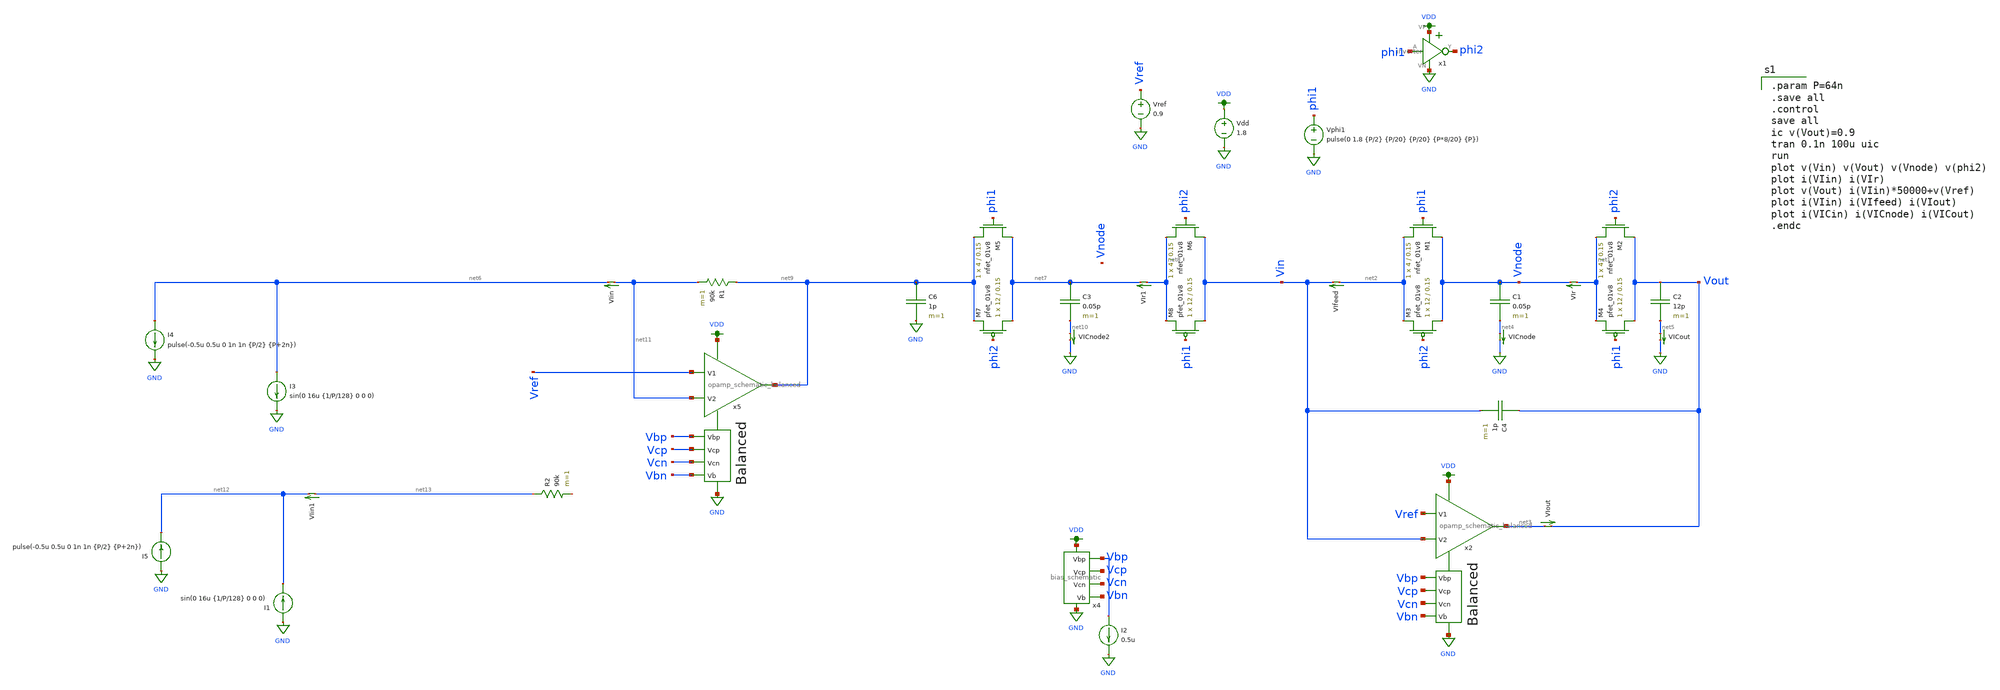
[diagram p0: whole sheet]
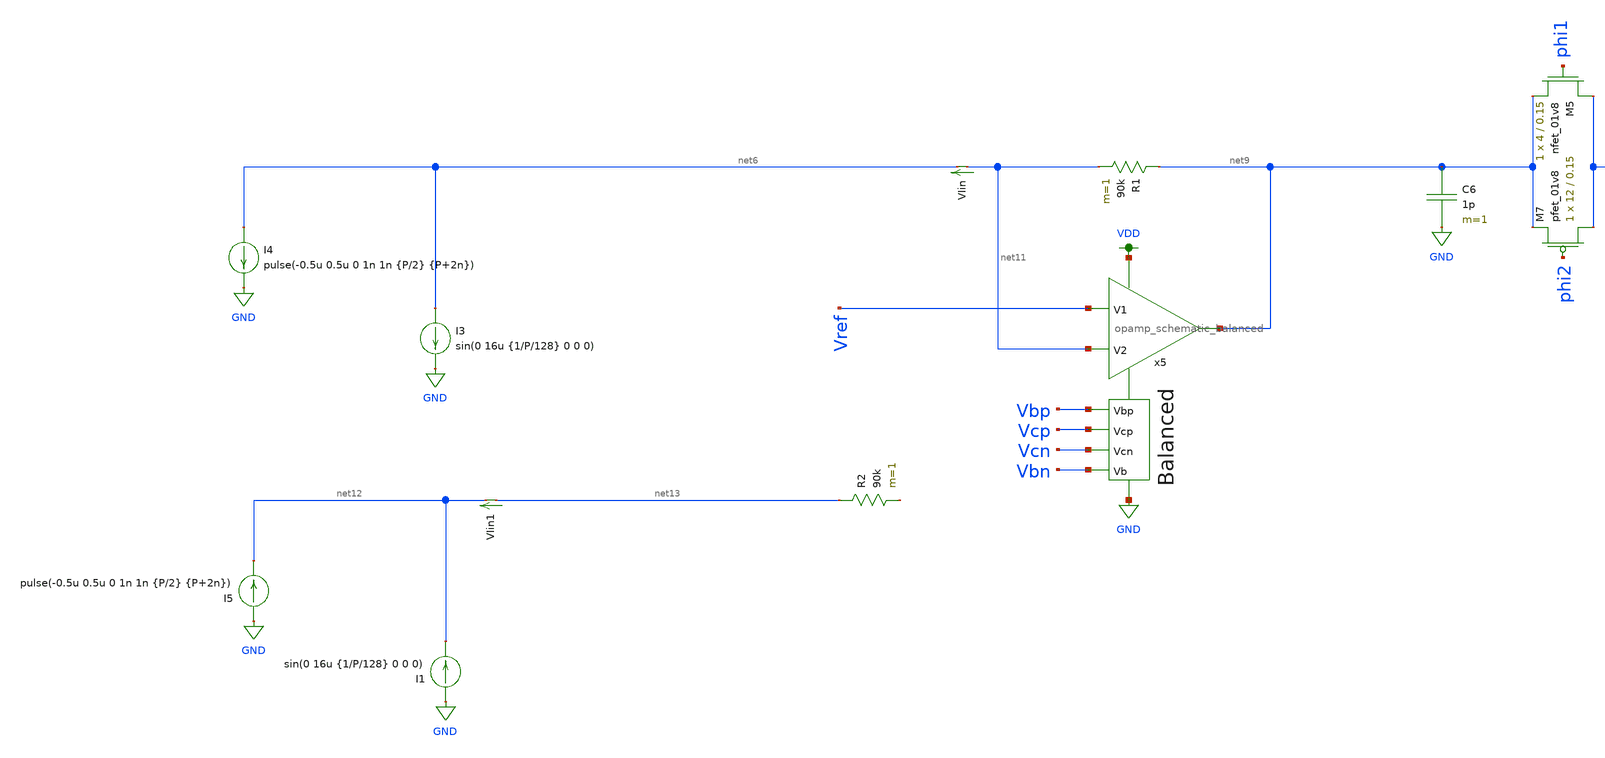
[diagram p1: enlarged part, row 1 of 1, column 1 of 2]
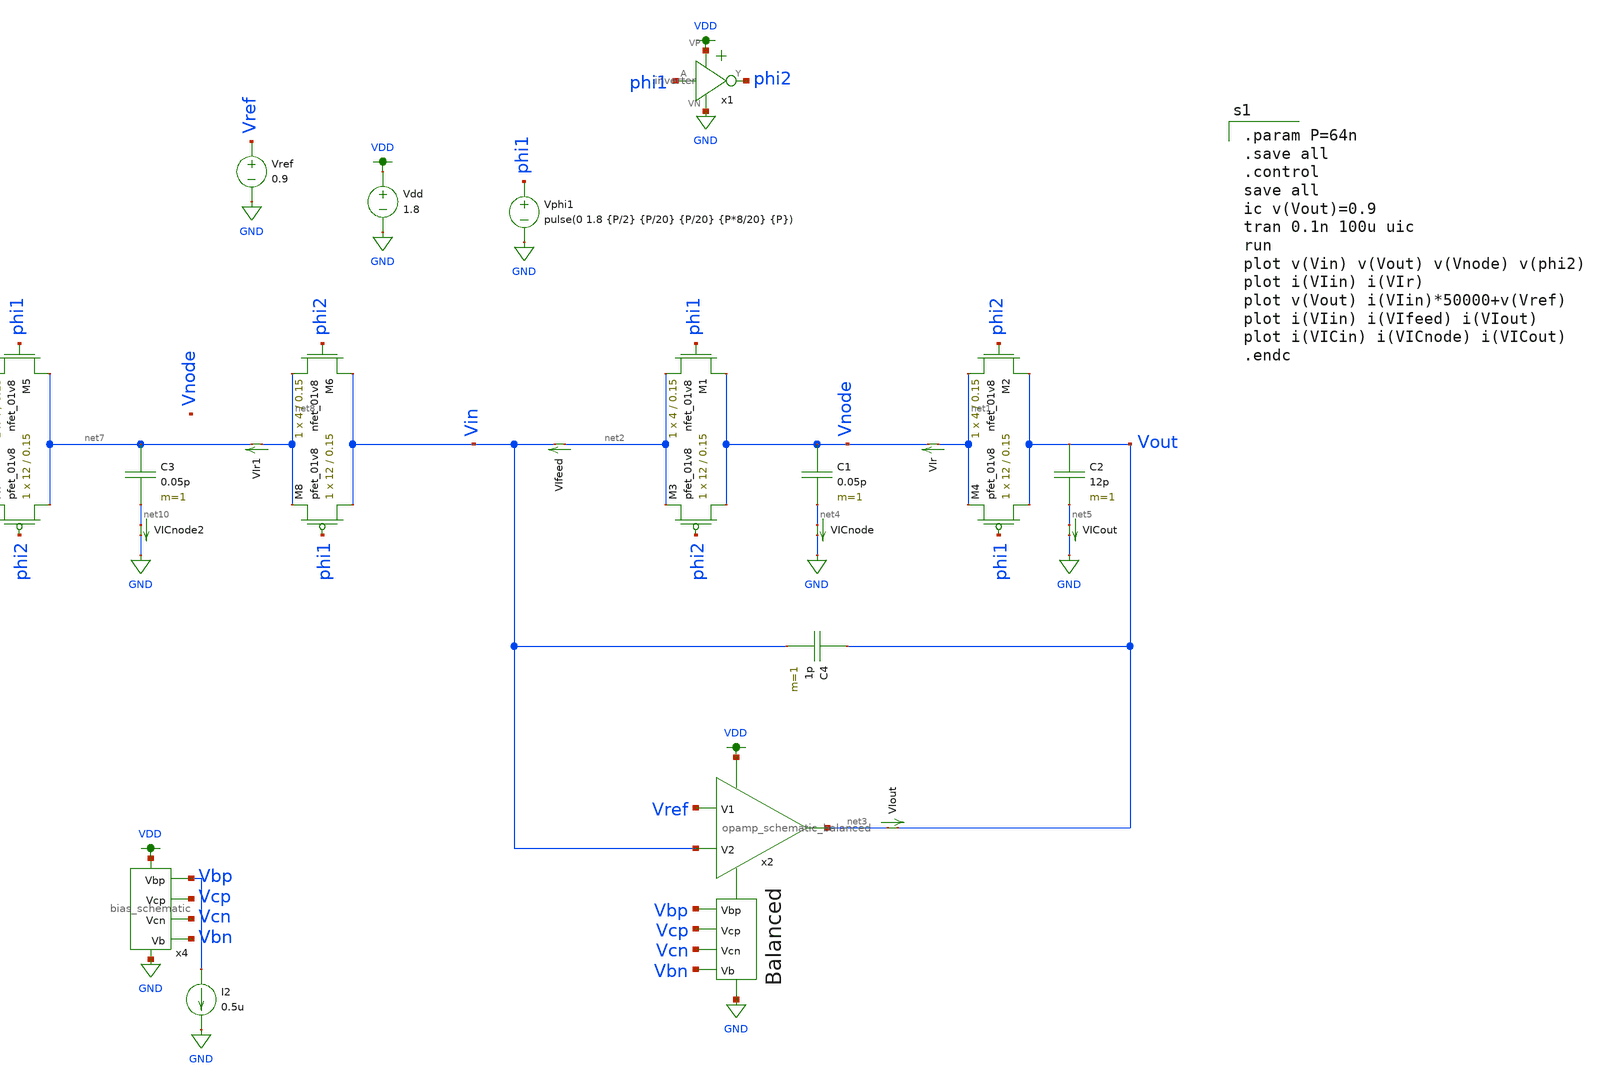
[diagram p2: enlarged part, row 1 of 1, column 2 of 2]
** sch_path: xschem/switched_capacitor/switched_capacitor_iv_lpf_third_order_diff_input.sch
**.subckt switched_capacitor_iv_lpf_third_order_diff_input
C1 Vnode net4 0.05p m=1
XM1 Vnode phi1 net2 GND sky130_fd_pr__nfet_01v8 L=0.15 W=4 nf=1 ad='int((nf+1)/2) * W/nf * 0.29' as='int((nf+2)/2) * W/nf * 0.29'
+ pd='2*int((nf+1)/2) * (W/nf + 0.29)' ps='2*int((nf+2)/2) * (W/nf + 0.29)' nrd='0.29 / W' nrs='0.29 / W'
+ sa=0 sb=0 sd=0 mult=1 m=1
XM2 Vout phi2 net1 GND sky130_fd_pr__nfet_01v8 L=0.15 W=4 nf=1 ad='int((nf+1)/2) * W/nf * 0.29' as='int((nf+2)/2) * W/nf * 0.29'
+ pd='2*int((nf+1)/2) * (W/nf + 0.29)' ps='2*int((nf+2)/2) * (W/nf + 0.29)' nrd='0.29 / W' nrs='0.29 / W'
+ sa=0 sb=0 sd=0 mult=1 m=1
Vphi1 phi1 GND pulse(0 1.8 {P/2} {P/20} {P/20} {P*8/20} {P})
Vdd VDD GND 1.8
C2 Vout net5 12p m=1
XM3 Vnode phi2 net2 VDD sky130_fd_pr__pfet_01v8 L=0.15 W=12 nf=1 ad='int((nf+1)/2) * W/nf * 0.29' as='int((nf+2)/2) * W/nf * 0.29'
+ pd='2*int((nf+1)/2) * (W/nf + 0.29)' ps='2*int((nf+2)/2) * (W/nf + 0.29)' nrd='0.29 / W' nrs='0.29 / W'
+ sa=0 sb=0 sd=0 mult=1 m=1
XM4 Vout phi1 net1 VDD sky130_fd_pr__pfet_01v8 L=0.15 W=12 nf=1 ad='int((nf+1)/2) * W/nf * 0.29' as='int((nf+2)/2) * W/nf * 0.29'
+ pd='2*int((nf+1)/2) * (W/nf + 0.29)' ps='2*int((nf+2)/2) * (W/nf + 0.29)' nrd='0.29 / W' nrs='0.29 / W'
+ sa=0 sb=0 sd=0 mult=1 m=1
x1 VDD phi1 phi2 GND inverter
x4 VDD Vbp Vcp Vcn GND Vbn bias_schematic
Vref Vref GND 0.9
I2 Vbp GND 0.5u
VIin net11 net6 0
.save i(viin)
VIr net1 Vnode 0
.save i(vir)
VIout net3 Vout 0
.save i(viout)
VICnode net4 GND 0
.save i(vicnode)
VICout net5 GND 0
.save i(vicout)
VIfeed net2 Vin 0
.save i(vifeed)
C4 Vout Vin 1p m=1
x2 VDD Vbp Vcp net3 Vref Vin Vcn Vbn GND opamp_schematic_balanced
I3 net6 GND sin(0 16u {1/P/128} 0 0 0)
C3 net7 net10 0.05p m=1
XM5 net7 phi1 net9 GND sky130_fd_pr__nfet_01v8 L=0.15 W=4 nf=1 ad='int((nf+1)/2) * W/nf * 0.29' as='int((nf+2)/2) * W/nf * 0.29'
+ pd='2*int((nf+1)/2) * (W/nf + 0.29)' ps='2*int((nf+2)/2) * (W/nf + 0.29)' nrd='0.29 / W' nrs='0.29 / W'
+ sa=0 sb=0 sd=0 mult=1 m=1
XM6 Vin phi2 net8 GND sky130_fd_pr__nfet_01v8 L=0.15 W=4 nf=1 ad='int((nf+1)/2) * W/nf * 0.29' as='int((nf+2)/2) * W/nf * 0.29'
+ pd='2*int((nf+1)/2) * (W/nf + 0.29)' ps='2*int((nf+2)/2) * (W/nf + 0.29)' nrd='0.29 / W' nrs='0.29 / W'
+ sa=0 sb=0 sd=0 mult=1 m=1
XM7 net7 phi2 net9 VDD sky130_fd_pr__pfet_01v8 L=0.15 W=12 nf=1 ad='int((nf+1)/2) * W/nf * 0.29' as='int((nf+2)/2) * W/nf * 0.29'
+ pd='2*int((nf+1)/2) * (W/nf + 0.29)' ps='2*int((nf+2)/2) * (W/nf + 0.29)' nrd='0.29 / W' nrs='0.29 / W'
+ sa=0 sb=0 sd=0 mult=1 m=1
XM8 Vin phi1 net8 VDD sky130_fd_pr__pfet_01v8 L=0.15 W=12 nf=1 ad='int((nf+1)/2) * W/nf * 0.29' as='int((nf+2)/2) * W/nf * 0.29'
+ pd='2*int((nf+1)/2) * (W/nf + 0.29)' ps='2*int((nf+2)/2) * (W/nf + 0.29)' nrd='0.29 / W' nrs='0.29 / W'
+ sa=0 sb=0 sd=0 mult=1 m=1
VIr1 net8 net7 0
.save i(vir1)
VICnode2 net10 GND 0
.save i(vicnode2)
C6 net9 GND 1p m=1
I4 net6 GND pulse(-0.5u 0.5u 0 1n 1n {P/2} {P+2n})
x5 VDD Vbp Vcp net9 Vref net11 Vcn Vbn GND opamp_schematic_balanced
R1 net9 net11 90k m=1
I1 GND net12 sin(0 16u {1/P/128} 0 0 0)
I5 GND net12 pulse(-0.5u 0.5u 0 1n 1n {P/2} {P+2n})
R2 net13 net14 90k m=1
VIin1 net13 net12 0
.save i(viin1)
**** begin user architecture code

.option wnflag=1
.param MC_SWITCH=0.0
.lib ~/skywater/skywater-pdk/libraries/sky130_fd_pr_ngspice/latest/models/sky130.lib.spice tt


.param P=64n
.save all
.control
save all
ic v(Vout)=0.9
tran 0.1n 100u uic
run
plot v(Vin) v(Vout) v(Vnode) v(phi2)
plot i(VIin) i(VIr)
plot v(Vout) i(VIin)*50000+v(Vref)
plot i(VIin) i(VIfeed) i(VIout)
plot i(VICin) i(VICnode) i(VICout)
.endc

**** end user architecture code
**.ends

* expanding   symbol:  /home/madvlsi/dev/git/magic-dds/xschem/other_project_files/inverter.sym # of
*+ pins=4
** sym_path: xschem/other_project_files/inverter.sym
** sch_path: xschem/other_project_files/inverter.sch
.subckt inverter VP A Y VN
*.iopin VP
*.iopin VN
*.ipin A
*.opin Y
XM1 Y A VN VN sky130_fd_pr__nfet_01v8 L=0.15 W=1 nf=1 ad='int((nf+1)/2) * W/nf * 0.29' as='int((nf+2)/2) * W/nf * 0.29'
+ pd='2*int((nf+1)/2) * (W/nf + 0.29)' ps='2*int((nf+2)/2) * (W/nf + 0.29)' nrd='0.29 / W' nrs='0.29 / W'
+ sa=0 sb=0 sd=0 mult=1 m=1
XM2 Y A VP VP sky130_fd_pr__pfet_01v8 L=0.15 W=4 nf=1 ad='int((nf+1)/2) * W/nf * 0.29' as='int((nf+2)/2) * W/nf * 0.29'
+ pd='2*int((nf+1)/2) * (W/nf + 0.29)' ps='2*int((nf+2)/2) * (W/nf + 0.29)' nrd='0.29 / W' nrs='0.29 / W'
+ sa=0 sb=0 sd=0 mult=1 m=1
.ends


* expanding   symbol:  /home/madvlsi/dev/git/magic-dds/xschem/other_project_files/bias_schematic.sym
*+ # of pins=6
** sym_path: xschem/other_project_files/bias_schematic.sym
** sch_path: xschem/other_project_files/bias_schematic.sch
.subckt bias_schematic VP Vbp Vcp Vcn VN Vb
*.iopin VP
*.iopin VN
*.opin Vcp
*.iopin Vbp
*.opin Vcn
*.opin Vb
XM1a net2 net2 net1 GND sky130_fd_pr__nfet_01v8 L=0.5 W=3 nf=1 ad='int((nf+1)/2) * W/nf * 0.29' as='int((nf+2)/2) * W/nf * 0.29'
+ pd='2*int((nf+1)/2) * (W/nf + 0.29)' ps='2*int((nf+2)/2) * (W/nf + 0.29)' nrd='0.29 / W' nrs='0.29 / W'
+ sa=0 sb=0 sd=0 mult=1 m=1
XM1b net2 net2 net1 GND sky130_fd_pr__nfet_01v8 L=0.5 W=3 nf=1 ad='int((nf+1)/2) * W/nf * 0.29' as='int((nf+2)/2) * W/nf * 0.29'
+ pd='2*int((nf+1)/2) * (W/nf + 0.29)' ps='2*int((nf+2)/2) * (W/nf + 0.29)' nrd='0.29 / W' nrs='0.29 / W'
+ sa=0 sb=0 sd=0 mult=1 m=1
XM1c net2 net2 net1 GND sky130_fd_pr__nfet_01v8 L=0.5 W=3 nf=1 ad='int((nf+1)/2) * W/nf * 0.29' as='int((nf+2)/2) * W/nf * 0.29'
+ pd='2*int((nf+1)/2) * (W/nf + 0.29)' ps='2*int((nf+2)/2) * (W/nf + 0.29)' nrd='0.29 / W' nrs='0.29 / W'
+ sa=0 sb=0 sd=0 mult=1 m=1
XM1d net2 net2 net1 GND sky130_fd_pr__nfet_01v8 L=0.5 W=3 nf=1 ad='int((nf+1)/2) * W/nf * 0.29' as='int((nf+2)/2) * W/nf * 0.29'
+ pd='2*int((nf+1)/2) * (W/nf + 0.29)' ps='2*int((nf+2)/2) * (W/nf + 0.29)' nrd='0.29 / W' nrs='0.29 / W'
+ sa=0 sb=0 sd=0 mult=1 m=1
XM2a VN net2 net1 GND sky130_fd_pr__nfet_01v8 L=0.5 W=3 nf=1 ad='int((nf+1)/2) * W/nf * 0.29' as='int((nf+2)/2) * W/nf * 0.29'
+ pd='2*int((nf+1)/2) * (W/nf + 0.29)' ps='2*int((nf+2)/2) * (W/nf + 0.29)' nrd='0.29 / W' nrs='0.29 / W'
+ sa=0 sb=0 sd=0 mult=1 m=1
XM2b VN net2 net1 GND sky130_fd_pr__nfet_01v8 L=0.5 W=3 nf=1 ad='int((nf+1)/2) * W/nf * 0.29' as='int((nf+2)/2) * W/nf * 0.29'
+ pd='2*int((nf+1)/2) * (W/nf + 0.29)' ps='2*int((nf+2)/2) * (W/nf + 0.29)' nrd='0.29 / W' nrs='0.29 / W'
+ sa=0 sb=0 sd=0 mult=1 m=1
XM2c VN net2 net1 GND sky130_fd_pr__nfet_01v8 L=0.5 W=3 nf=1 ad='int((nf+1)/2) * W/nf * 0.29' as='int((nf+2)/2) * W/nf * 0.29'
+ pd='2*int((nf+1)/2) * (W/nf + 0.29)' ps='2*int((nf+2)/2) * (W/nf + 0.29)' nrd='0.29 / W' nrs='0.29 / W'
+ sa=0 sb=0 sd=0 mult=1 m=1
XM2d VN net2 net1 GND sky130_fd_pr__nfet_01v8 L=0.5 W=3 nf=1 ad='int((nf+1)/2) * W/nf * 0.29' as='int((nf+2)/2) * W/nf * 0.29'
+ pd='2*int((nf+1)/2) * (W/nf + 0.29)' ps='2*int((nf+2)/2) * (W/nf + 0.29)' nrd='0.29 / W' nrs='0.29 / W'
+ sa=0 sb=0 sd=0 mult=1 m=1
XM3a net2 Vbp net7 VDD sky130_fd_pr__pfet_01v8 L=0.5 W=3 nf=1 ad='int((nf+1)/2) * W/nf * 0.29' as='int((nf+2)/2) * W/nf * 0.29'
+ pd='2*int((nf+1)/2) * (W/nf + 0.29)' ps='2*int((nf+2)/2) * (W/nf + 0.29)' nrd='0.29 / W' nrs='0.29 / W'
+ sa=0 sb=0 sd=0 mult=1 m=1
XM3b net7 Vbp net6 VDD sky130_fd_pr__pfet_01v8 L=0.5 W=3 nf=1 ad='int((nf+1)/2) * W/nf * 0.29' as='int((nf+2)/2) * W/nf * 0.29'
+ pd='2*int((nf+1)/2) * (W/nf + 0.29)' ps='2*int((nf+2)/2) * (W/nf + 0.29)' nrd='0.29 / W' nrs='0.29 / W'
+ sa=0 sb=0 sd=0 mult=1 m=1
XM3c net6 Vbp net5 VDD sky130_fd_pr__pfet_01v8 L=0.5 W=3 nf=1 ad='int((nf+1)/2) * W/nf * 0.29' as='int((nf+2)/2) * W/nf * 0.29'
+ pd='2*int((nf+1)/2) * (W/nf + 0.29)' ps='2*int((nf+2)/2) * (W/nf + 0.29)' nrd='0.29 / W' nrs='0.29 / W'
+ sa=0 sb=0 sd=0 mult=1 m=1
XM3d net5 Vbp VP VDD sky130_fd_pr__pfet_01v8 L=0.5 W=3 nf=1 ad='int((nf+1)/2) * W/nf * 0.29' as='int((nf+2)/2) * W/nf * 0.29'
+ pd='2*int((nf+1)/2) * (W/nf + 0.29)' ps='2*int((nf+2)/2) * (W/nf + 0.29)' nrd='0.29 / W' nrs='0.29 / W'
+ sa=0 sb=0 sd=0 mult=1 m=1
XM4a Vcn Vbp VP VDD sky130_fd_pr__pfet_01v8 L=0.5 W=3 nf=1 ad='int((nf+1)/2) * W/nf * 0.29' as='int((nf+2)/2) * W/nf * 0.29'
+ pd='2*int((nf+1)/2) * (W/nf + 0.29)' ps='2*int((nf+2)/2) * (W/nf + 0.29)' nrd='0.29 / W' nrs='0.29 / W'
+ sa=0 sb=0 sd=0 mult=1 m=1
XM4b Vcn Vbp VP VDD sky130_fd_pr__pfet_01v8 L=0.5 W=3 nf=1 ad='int((nf+1)/2) * W/nf * 0.29' as='int((nf+2)/2) * W/nf * 0.29'
+ pd='2*int((nf+1)/2) * (W/nf + 0.29)' ps='2*int((nf+2)/2) * (W/nf + 0.29)' nrd='0.29 / W' nrs='0.29 / W'
+ sa=0 sb=0 sd=0 mult=1 m=1
XM4c Vcn Vbp VP VDD sky130_fd_pr__pfet_01v8 L=0.5 W=3 nf=1 ad='int((nf+1)/2) * W/nf * 0.29' as='int((nf+2)/2) * W/nf * 0.29'
+ pd='2*int((nf+1)/2) * (W/nf + 0.29)' ps='2*int((nf+2)/2) * (W/nf + 0.29)' nrd='0.29 / W' nrs='0.29 / W'
+ sa=0 sb=0 sd=0 mult=1 m=1
XM4d Vcn Vbp VP VDD sky130_fd_pr__pfet_01v8 L=0.5 W=3 nf=1 ad='int((nf+1)/2) * W/nf * 0.29' as='int((nf+2)/2) * W/nf * 0.29'
+ pd='2*int((nf+1)/2) * (W/nf + 0.29)' ps='2*int((nf+2)/2) * (W/nf + 0.29)' nrd='0.29 / W' nrs='0.29 / W'
+ sa=0 sb=0 sd=0 mult=1 m=1
XM11a VP Vbp Vbp VDD sky130_fd_pr__pfet_01v8 L=0.5 W=3 nf=1 ad='int((nf+1)/2) * W/nf * 0.29' as='int((nf+2)/2) * W/nf * 0.29'
+ pd='2*int((nf+1)/2) * (W/nf + 0.29)' ps='2*int((nf+2)/2) * (W/nf + 0.29)' nrd='0.29 / W' nrs='0.29 / W'
+ sa=0 sb=0 sd=0 mult=1 m=1
XM11b VP Vbp Vbp VDD sky130_fd_pr__pfet_01v8 L=0.5 W=3 nf=1 ad='int((nf+1)/2) * W/nf * 0.29' as='int((nf+2)/2) * W/nf * 0.29'
+ pd='2*int((nf+1)/2) * (W/nf + 0.29)' ps='2*int((nf+2)/2) * (W/nf + 0.29)' nrd='0.29 / W' nrs='0.29 / W'
+ sa=0 sb=0 sd=0 mult=1 m=1
XM11c VP Vbp Vbp VDD sky130_fd_pr__pfet_01v8 L=0.5 W=3 nf=1 ad='int((nf+1)/2) * W/nf * 0.29' as='int((nf+2)/2) * W/nf * 0.29'
+ pd='2*int((nf+1)/2) * (W/nf + 0.29)' ps='2*int((nf+2)/2) * (W/nf + 0.29)' nrd='0.29 / W' nrs='0.29 / W'
+ sa=0 sb=0 sd=0 mult=1 m=1
XM11d VP Vbp Vbp VDD sky130_fd_pr__pfet_01v8 L=0.5 W=3 nf=1 ad='int((nf+1)/2) * W/nf * 0.29' as='int((nf+2)/2) * W/nf * 0.29'
+ pd='2*int((nf+1)/2) * (W/nf + 0.29)' ps='2*int((nf+2)/2) * (W/nf + 0.29)' nrd='0.29 / W' nrs='0.29 / W'
+ sa=0 sb=0 sd=0 mult=1 m=1
XM5a net1 Vcn Vcn GND sky130_fd_pr__nfet_01v8 L=0.5 W=3 nf=1 ad='int((nf+1)/2) * W/nf * 0.29' as='int((nf+2)/2) * W/nf * 0.29'
+ pd='2*int((nf+1)/2) * (W/nf + 0.29)' ps='2*int((nf+2)/2) * (W/nf + 0.29)' nrd='0.29 / W' nrs='0.29 / W'
+ sa=0 sb=0 sd=0 mult=1 m=1
XM5b net1 Vcn Vcn GND sky130_fd_pr__nfet_01v8 L=0.5 W=3 nf=1 ad='int((nf+1)/2) * W/nf * 0.29' as='int((nf+2)/2) * W/nf * 0.29'
+ pd='2*int((nf+1)/2) * (W/nf + 0.29)' ps='2*int((nf+2)/2) * (W/nf + 0.29)' nrd='0.29 / W' nrs='0.29 / W'
+ sa=0 sb=0 sd=0 mult=1 m=1
XM5c net1 Vcn Vcn GND sky130_fd_pr__nfet_01v8 L=0.5 W=3 nf=1 ad='int((nf+1)/2) * W/nf * 0.29' as='int((nf+2)/2) * W/nf * 0.29'
+ pd='2*int((nf+1)/2) * (W/nf + 0.29)' ps='2*int((nf+2)/2) * (W/nf + 0.29)' nrd='0.29 / W' nrs='0.29 / W'
+ sa=0 sb=0 sd=0 mult=1 m=1
XM5d net1 Vcn Vcn GND sky130_fd_pr__nfet_01v8 L=0.5 W=3 nf=1 ad='int((nf+1)/2) * W/nf * 0.29' as='int((nf+2)/2) * W/nf * 0.29'
+ pd='2*int((nf+1)/2) * (W/nf + 0.29)' ps='2*int((nf+2)/2) * (W/nf + 0.29)' nrd='0.29 / W' nrs='0.29 / W'
+ sa=0 sb=0 sd=0 mult=1 m=1
XM8a net10 Vb net3 GND sky130_fd_pr__nfet_01v8 L=0.5 W=3 nf=1 ad='int((nf+1)/2) * W/nf * 0.29' as='int((nf+2)/2) * W/nf * 0.29'
+ pd='2*int((nf+1)/2) * (W/nf + 0.29)' ps='2*int((nf+2)/2) * (W/nf + 0.29)' nrd='0.29 / W' nrs='0.29 / W'
+ sa=0 sb=0 sd=0 mult=1 m=1
XM8b net9 Vb net10 GND sky130_fd_pr__nfet_01v8 L=0.5 W=3 nf=1 ad='int((nf+1)/2) * W/nf * 0.29' as='int((nf+2)/2) * W/nf * 0.29'
+ pd='2*int((nf+1)/2) * (W/nf + 0.29)' ps='2*int((nf+2)/2) * (W/nf + 0.29)' nrd='0.29 / W' nrs='0.29 / W'
+ sa=0 sb=0 sd=0 mult=1 m=1
XM8c net8 Vb net9 GND sky130_fd_pr__nfet_01v8 L=0.5 W=3 nf=1 ad='int((nf+1)/2) * W/nf * 0.29' as='int((nf+2)/2) * W/nf * 0.29'
+ pd='2*int((nf+1)/2) * (W/nf + 0.29)' ps='2*int((nf+2)/2) * (W/nf + 0.29)' nrd='0.29 / W' nrs='0.29 / W'
+ sa=0 sb=0 sd=0 mult=1 m=1
XM8d VN Vb net8 GND sky130_fd_pr__nfet_01v8 L=0.5 W=3 nf=1 ad='int((nf+1)/2) * W/nf * 0.29' as='int((nf+2)/2) * W/nf * 0.29'
+ pd='2*int((nf+1)/2) * (W/nf + 0.29)' ps='2*int((nf+2)/2) * (W/nf + 0.29)' nrd='0.29 / W' nrs='0.29 / W'
+ sa=0 sb=0 sd=0 mult=1 m=1
XM6a net3 net3 net4 VDD sky130_fd_pr__pfet_01v8 L=0.5 W=3 nf=1 ad='int((nf+1)/2) * W/nf * 0.29' as='int((nf+2)/2) * W/nf * 0.29'
+ pd='2*int((nf+1)/2) * (W/nf + 0.29)' ps='2*int((nf+2)/2) * (W/nf + 0.29)' nrd='0.29 / W' nrs='0.29 / W'
+ sa=0 sb=0 sd=0 mult=1 m=1
XM6b net3 net3 net4 VDD sky130_fd_pr__pfet_01v8 L=0.5 W=3 nf=1 ad='int((nf+1)/2) * W/nf * 0.29' as='int((nf+2)/2) * W/nf * 0.29'
+ pd='2*int((nf+1)/2) * (W/nf + 0.29)' ps='2*int((nf+2)/2) * (W/nf + 0.29)' nrd='0.29 / W' nrs='0.29 / W'
+ sa=0 sb=0 sd=0 mult=1 m=1
XM6c net3 net3 net4 VDD sky130_fd_pr__pfet_01v8 L=0.5 W=3 nf=1 ad='int((nf+1)/2) * W/nf * 0.29' as='int((nf+2)/2) * W/nf * 0.29'
+ pd='2*int((nf+1)/2) * (W/nf + 0.29)' ps='2*int((nf+2)/2) * (W/nf + 0.29)' nrd='0.29 / W' nrs='0.29 / W'
+ sa=0 sb=0 sd=0 mult=1 m=1
XM6d net3 net3 net4 VDD sky130_fd_pr__pfet_01v8 L=0.5 W=3 nf=1 ad='int((nf+1)/2) * W/nf * 0.29' as='int((nf+2)/2) * W/nf * 0.29'
+ pd='2*int((nf+1)/2) * (W/nf + 0.29)' ps='2*int((nf+2)/2) * (W/nf + 0.29)' nrd='0.29 / W' nrs='0.29 / W'
+ sa=0 sb=0 sd=0 mult=1 m=1
XM7a net4 net3 VP VDD sky130_fd_pr__pfet_01v8 L=0.5 W=3 nf=1 ad='int((nf+1)/2) * W/nf * 0.29' as='int((nf+2)/2) * W/nf * 0.29'
+ pd='2*int((nf+1)/2) * (W/nf + 0.29)' ps='2*int((nf+2)/2) * (W/nf + 0.29)' nrd='0.29 / W' nrs='0.29 / W'
+ sa=0 sb=0 sd=0 mult=1 m=1
XM7b net4 net3 VP VDD sky130_fd_pr__pfet_01v8 L=0.5 W=3 nf=1 ad='int((nf+1)/2) * W/nf * 0.29' as='int((nf+2)/2) * W/nf * 0.29'
+ pd='2*int((nf+1)/2) * (W/nf + 0.29)' ps='2*int((nf+2)/2) * (W/nf + 0.29)' nrd='0.29 / W' nrs='0.29 / W'
+ sa=0 sb=0 sd=0 mult=1 m=1
XM7c net4 net3 VP VDD sky130_fd_pr__pfet_01v8 L=0.5 W=3 nf=1 ad='int((nf+1)/2) * W/nf * 0.29' as='int((nf+2)/2) * W/nf * 0.29'
+ pd='2*int((nf+1)/2) * (W/nf + 0.29)' ps='2*int((nf+2)/2) * (W/nf + 0.29)' nrd='0.29 / W' nrs='0.29 / W'
+ sa=0 sb=0 sd=0 mult=1 m=1
XM7d net4 net3 VP VDD sky130_fd_pr__pfet_01v8 L=0.5 W=3 nf=1 ad='int((nf+1)/2) * W/nf * 0.29' as='int((nf+2)/2) * W/nf * 0.29'
+ pd='2*int((nf+1)/2) * (W/nf + 0.29)' ps='2*int((nf+2)/2) * (W/nf + 0.29)' nrd='0.29 / W' nrs='0.29 / W'
+ sa=0 sb=0 sd=0 mult=1 m=1
XM10d net4 Vcp Vcp VDD sky130_fd_pr__pfet_01v8 L=0.5 W=3 nf=1 ad='int((nf+1)/2) * W/nf * 0.29' as='int((nf+2)/2) * W/nf * 0.29'
+ pd='2*int((nf+1)/2) * (W/nf + 0.29)' ps='2*int((nf+2)/2) * (W/nf + 0.29)' nrd='0.29 / W' nrs='0.29 / W'
+ sa=0 sb=0 sd=0 mult=1 m=1
XM10c net4 Vcp Vcp VDD sky130_fd_pr__pfet_01v8 L=0.5 W=3 nf=1 ad='int((nf+1)/2) * W/nf * 0.29' as='int((nf+2)/2) * W/nf * 0.29'
+ pd='2*int((nf+1)/2) * (W/nf + 0.29)' ps='2*int((nf+2)/2) * (W/nf + 0.29)' nrd='0.29 / W' nrs='0.29 / W'
+ sa=0 sb=0 sd=0 mult=1 m=1
XM10b net4 Vcp Vcp VDD sky130_fd_pr__pfet_01v8 L=0.5 W=3 nf=1 ad='int((nf+1)/2) * W/nf * 0.29' as='int((nf+2)/2) * W/nf * 0.29'
+ pd='2*int((nf+1)/2) * (W/nf + 0.29)' ps='2*int((nf+2)/2) * (W/nf + 0.29)' nrd='0.29 / W' nrs='0.29 / W'
+ sa=0 sb=0 sd=0 mult=1 m=1
XM10a net4 Vcp Vcp VDD sky130_fd_pr__pfet_01v8 L=0.5 W=3 nf=1 ad='int((nf+1)/2) * W/nf * 0.29' as='int((nf+2)/2) * W/nf * 0.29'
+ pd='2*int((nf+1)/2) * (W/nf + 0.29)' ps='2*int((nf+2)/2) * (W/nf + 0.29)' nrd='0.29 / W' nrs='0.29 / W'
+ sa=0 sb=0 sd=0 mult=1 m=1
XM9a VN Vb Vcp GND sky130_fd_pr__nfet_01v8 L=0.5 W=3 nf=1 ad='int((nf+1)/2) * W/nf * 0.29' as='int((nf+2)/2) * W/nf * 0.29'
+ pd='2*int((nf+1)/2) * (W/nf + 0.29)' ps='2*int((nf+2)/2) * (W/nf + 0.29)' nrd='0.29 / W' nrs='0.29 / W'
+ sa=0 sb=0 sd=0 mult=1 m=1
XM9b VN Vb Vcp GND sky130_fd_pr__nfet_01v8 L=0.5 W=3 nf=1 ad='int((nf+1)/2) * W/nf * 0.29' as='int((nf+2)/2) * W/nf * 0.29'
+ pd='2*int((nf+1)/2) * (W/nf + 0.29)' ps='2*int((nf+2)/2) * (W/nf + 0.29)' nrd='0.29 / W' nrs='0.29 / W'
+ sa=0 sb=0 sd=0 mult=1 m=1
XM9c VN Vb Vcp GND sky130_fd_pr__nfet_01v8 L=0.5 W=3 nf=1 ad='int((nf+1)/2) * W/nf * 0.29' as='int((nf+2)/2) * W/nf * 0.29'
+ pd='2*int((nf+1)/2) * (W/nf + 0.29)' ps='2*int((nf+2)/2) * (W/nf + 0.29)' nrd='0.29 / W' nrs='0.29 / W'
+ sa=0 sb=0 sd=0 mult=1 m=1
XM9d VN Vb Vcp GND sky130_fd_pr__nfet_01v8 L=0.5 W=3 nf=1 ad='int((nf+1)/2) * W/nf * 0.29' as='int((nf+2)/2) * W/nf * 0.29'
+ pd='2*int((nf+1)/2) * (W/nf + 0.29)' ps='2*int((nf+2)/2) * (W/nf + 0.29)' nrd='0.29 / W' nrs='0.29 / W'
+ sa=0 sb=0 sd=0 mult=1 m=1
XM12a VN Vb Vb GND sky130_fd_pr__nfet_01v8 L=0.5 W=3 nf=1 ad='int((nf+1)/2) * W/nf * 0.29' as='int((nf+2)/2) * W/nf * 0.29'
+ pd='2*int((nf+1)/2) * (W/nf + 0.29)' ps='2*int((nf+2)/2) * (W/nf + 0.29)' nrd='0.29 / W' nrs='0.29 / W'
+ sa=0 sb=0 sd=0 mult=1 m=1
XM12b VN Vb Vb GND sky130_fd_pr__nfet_01v8 L=0.5 W=3 nf=1 ad='int((nf+1)/2) * W/nf * 0.29' as='int((nf+2)/2) * W/nf * 0.29'
+ pd='2*int((nf+1)/2) * (W/nf + 0.29)' ps='2*int((nf+2)/2) * (W/nf + 0.29)' nrd='0.29 / W' nrs='0.29 / W'
+ sa=0 sb=0 sd=0 mult=1 m=1
XM12c VN Vb Vb GND sky130_fd_pr__nfet_01v8 L=0.5 W=3 nf=1 ad='int((nf+1)/2) * W/nf * 0.29' as='int((nf+2)/2) * W/nf * 0.29'
+ pd='2*int((nf+1)/2) * (W/nf + 0.29)' ps='2*int((nf+2)/2) * (W/nf + 0.29)' nrd='0.29 / W' nrs='0.29 / W'
+ sa=0 sb=0 sd=0 mult=1 m=1
XM12d VN Vb Vb GND sky130_fd_pr__nfet_01v8 L=0.5 W=3 nf=1 ad='int((nf+1)/2) * W/nf * 0.29' as='int((nf+2)/2) * W/nf * 0.29'
+ pd='2*int((nf+1)/2) * (W/nf + 0.29)' ps='2*int((nf+2)/2) * (W/nf + 0.29)' nrd='0.29 / W' nrs='0.29 / W'
+ sa=0 sb=0 sd=0 mult=1 m=1
XM1 Vb Vbp VP VDD sky130_fd_pr__pfet_01v8 L=0.5 W=3 nf=1 ad='int((nf+1)/2) * W/nf * 0.29' as='int((nf+2)/2) * W/nf * 0.29'
+ pd='2*int((nf+1)/2) * (W/nf + 0.29)' ps='2*int((nf+2)/2) * (W/nf + 0.29)' nrd='0.29 / W' nrs='0.29 / W'
+ sa=0 sb=0 sd=0 mult=1 m=1
XM2 Vb Vbp VP VDD sky130_fd_pr__pfet_01v8 L=0.5 W=3 nf=1 ad='int((nf+1)/2) * W/nf * 0.29' as='int((nf+2)/2) * W/nf * 0.29'
+ pd='2*int((nf+1)/2) * (W/nf + 0.29)' ps='2*int((nf+2)/2) * (W/nf + 0.29)' nrd='0.29 / W' nrs='0.29 / W'
+ sa=0 sb=0 sd=0 mult=1 m=1
XM3 Vb Vbp VP VDD sky130_fd_pr__pfet_01v8 L=0.5 W=3 nf=1 ad='int((nf+1)/2) * W/nf * 0.29' as='int((nf+2)/2) * W/nf * 0.29'
+ pd='2*int((nf+1)/2) * (W/nf + 0.29)' ps='2*int((nf+2)/2) * (W/nf + 0.29)' nrd='0.29 / W' nrs='0.29 / W'
+ sa=0 sb=0 sd=0 mult=1 m=1
XM4 Vb Vbp VP VDD sky130_fd_pr__pfet_01v8 L=0.5 W=3 nf=1 ad='int((nf+1)/2) * W/nf * 0.29' as='int((nf+2)/2) * W/nf * 0.29'
+ pd='2*int((nf+1)/2) * (W/nf + 0.29)' ps='2*int((nf+2)/2) * (W/nf + 0.29)' nrd='0.29 / W' nrs='0.29 / W'
+ sa=0 sb=0 sd=0 mult=1 m=1
XM1e net2 net2 net1 GND sky130_fd_pr__nfet_01v8 L=0.5 W=3 nf=1 ad='int((nf+1)/2) * W/nf * 0.29' as='int((nf+2)/2) * W/nf * 0.29'
+ pd='2*int((nf+1)/2) * (W/nf + 0.29)' ps='2*int((nf+2)/2) * (W/nf + 0.29)' nrd='0.29 / W' nrs='0.29 / W'
+ sa=0 sb=0 sd=0 mult=1 m=1
XM1f net2 net2 net1 GND sky130_fd_pr__nfet_01v8 L=0.5 W=3 nf=1 ad='int((nf+1)/2) * W/nf * 0.29' as='int((nf+2)/2) * W/nf * 0.29'
+ pd='2*int((nf+1)/2) * (W/nf + 0.29)' ps='2*int((nf+2)/2) * (W/nf + 0.29)' nrd='0.29 / W' nrs='0.29 / W'
+ sa=0 sb=0 sd=0 mult=1 m=1
XM1g net2 net2 net1 GND sky130_fd_pr__nfet_01v8 L=0.5 W=3 nf=1 ad='int((nf+1)/2) * W/nf * 0.29' as='int((nf+2)/2) * W/nf * 0.29'
+ pd='2*int((nf+1)/2) * (W/nf + 0.29)' ps='2*int((nf+2)/2) * (W/nf + 0.29)' nrd='0.29 / W' nrs='0.29 / W'
+ sa=0 sb=0 sd=0 mult=1 m=1
XM1h net2 net2 net1 GND sky130_fd_pr__nfet_01v8 L=0.5 W=3 nf=1 ad='int((nf+1)/2) * W/nf * 0.29' as='int((nf+2)/2) * W/nf * 0.29'
+ pd='2*int((nf+1)/2) * (W/nf + 0.29)' ps='2*int((nf+2)/2) * (W/nf + 0.29)' nrd='0.29 / W' nrs='0.29 / W'
+ sa=0 sb=0 sd=0 mult=1 m=1
XM6e net3 net3 net4 VDD sky130_fd_pr__pfet_01v8 L=0.5 W=3 nf=1 ad='int((nf+1)/2) * W/nf * 0.29' as='int((nf+2)/2) * W/nf * 0.29'
+ pd='2*int((nf+1)/2) * (W/nf + 0.29)' ps='2*int((nf+2)/2) * (W/nf + 0.29)' nrd='0.29 / W' nrs='0.29 / W'
+ sa=0 sb=0 sd=0 mult=1 m=1
XM6f net3 net3 net4 VDD sky130_fd_pr__pfet_01v8 L=0.5 W=3 nf=1 ad='int((nf+1)/2) * W/nf * 0.29' as='int((nf+2)/2) * W/nf * 0.29'
+ pd='2*int((nf+1)/2) * (W/nf + 0.29)' ps='2*int((nf+2)/2) * (W/nf + 0.29)' nrd='0.29 / W' nrs='0.29 / W'
+ sa=0 sb=0 sd=0 mult=1 m=1
XM6g net3 net3 net4 VDD sky130_fd_pr__pfet_01v8 L=0.5 W=3 nf=1 ad='int((nf+1)/2) * W/nf * 0.29' as='int((nf+2)/2) * W/nf * 0.29'
+ pd='2*int((nf+1)/2) * (W/nf + 0.29)' ps='2*int((nf+2)/2) * (W/nf + 0.29)' nrd='0.29 / W' nrs='0.29 / W'
+ sa=0 sb=0 sd=0 mult=1 m=1
XM6h net3 net3 net4 VDD sky130_fd_pr__pfet_01v8 L=0.5 W=3 nf=1 ad='int((nf+1)/2) * W/nf * 0.29' as='int((nf+2)/2) * W/nf * 0.29'
+ pd='2*int((nf+1)/2) * (W/nf + 0.29)' ps='2*int((nf+2)/2) * (W/nf + 0.29)' nrd='0.29 / W' nrs='0.29 / W'
+ sa=0 sb=0 sd=0 mult=1 m=1
XM1i net2 net2 net1 GND sky130_fd_pr__nfet_01v8 L=0.5 W=3 nf=1 ad='int((nf+1)/2) * W/nf * 0.29' as='int((nf+2)/2) * W/nf * 0.29'
+ pd='2*int((nf+1)/2) * (W/nf + 0.29)' ps='2*int((nf+2)/2) * (W/nf + 0.29)' nrd='0.29 / W' nrs='0.29 / W'
+ sa=0 sb=0 sd=0 mult=1 m=1
XM1j net2 net2 net1 GND sky130_fd_pr__nfet_01v8 L=0.5 W=3 nf=1 ad='int((nf+1)/2) * W/nf * 0.29' as='int((nf+2)/2) * W/nf * 0.29'
+ pd='2*int((nf+1)/2) * (W/nf + 0.29)' ps='2*int((nf+2)/2) * (W/nf + 0.29)' nrd='0.29 / W' nrs='0.29 / W'
+ sa=0 sb=0 sd=0 mult=1 m=1
XM1k net2 net2 net1 GND sky130_fd_pr__nfet_01v8 L=0.5 W=3 nf=1 ad='int((nf+1)/2) * W/nf * 0.29' as='int((nf+2)/2) * W/nf * 0.29'
+ pd='2*int((nf+1)/2) * (W/nf + 0.29)' ps='2*int((nf+2)/2) * (W/nf + 0.29)' nrd='0.29 / W' nrs='0.29 / W'
+ sa=0 sb=0 sd=0 mult=1 m=1
XM1l net2 net2 net1 GND sky130_fd_pr__nfet_01v8 L=0.5 W=3 nf=1 ad='int((nf+1)/2) * W/nf * 0.29' as='int((nf+2)/2) * W/nf * 0.29'
+ pd='2*int((nf+1)/2) * (W/nf + 0.29)' ps='2*int((nf+2)/2) * (W/nf + 0.29)' nrd='0.29 / W' nrs='0.29 / W'
+ sa=0 sb=0 sd=0 mult=1 m=1
XM6i net3 net3 net4 VDD sky130_fd_pr__pfet_01v8 L=0.5 W=3 nf=1 ad='int((nf+1)/2) * W/nf * 0.29' as='int((nf+2)/2) * W/nf * 0.29'
+ pd='2*int((nf+1)/2) * (W/nf + 0.29)' ps='2*int((nf+2)/2) * (W/nf + 0.29)' nrd='0.29 / W' nrs='0.29 / W'
+ sa=0 sb=0 sd=0 mult=1 m=1
XM6j net3 net3 net4 VDD sky130_fd_pr__pfet_01v8 L=0.5 W=3 nf=1 ad='int((nf+1)/2) * W/nf * 0.29' as='int((nf+2)/2) * W/nf * 0.29'
+ pd='2*int((nf+1)/2) * (W/nf + 0.29)' ps='2*int((nf+2)/2) * (W/nf + 0.29)' nrd='0.29 / W' nrs='0.29 / W'
+ sa=0 sb=0 sd=0 mult=1 m=1
XM6k net3 net3 net4 VDD sky130_fd_pr__pfet_01v8 L=0.5 W=3 nf=1 ad='int((nf+1)/2) * W/nf * 0.29' as='int((nf+2)/2) * W/nf * 0.29'
+ pd='2*int((nf+1)/2) * (W/nf + 0.29)' ps='2*int((nf+2)/2) * (W/nf + 0.29)' nrd='0.29 / W' nrs='0.29 / W'
+ sa=0 sb=0 sd=0 mult=1 m=1
XM6l net3 net3 net4 VDD sky130_fd_pr__pfet_01v8 L=0.5 W=3 nf=1 ad='int((nf+1)/2) * W/nf * 0.29' as='int((nf+2)/2) * W/nf * 0.29'
+ pd='2*int((nf+1)/2) * (W/nf + 0.29)' ps='2*int((nf+2)/2) * (W/nf + 0.29)' nrd='0.29 / W' nrs='0.29 / W'
+ sa=0 sb=0 sd=0 mult=1 m=1
.ends


* expanding   symbol:
*+  /home/madvlsi/dev/git/magic-dds/xschem/other_project_files/opamp_schematic_balanced.sym # of pins=9
** sym_path: xschem/other_project_files/opamp_schematic_balanced.sym
** sch_path: xschem/other_project_files/opamp_schematic_balanced.sch
.subckt opamp_schematic_balanced VP Vbp Vcp Vout V1 V2 Vcn Vb VN
*.ipin Vbp
*.ipin Vcp
*.ipin Vcn
*.ipin V2
*.ipin V1
*.ipin Vb
*.iopin VP
*.iopin VN
*.opin Vout
XM1a M1top V1 Vnode GND sky130_fd_pr__nfet_01v8 L=0.5 W=3 nf=1 ad='int((nf+1)/2) * W/nf * 0.29' as='int((nf+2)/2) * W/nf * 0.29'
+ pd='2*int((nf+1)/2) * (W/nf + 0.29)' ps='2*int((nf+2)/2) * (W/nf + 0.29)' nrd='0.29 / W' nrs='0.29 / W'
+ sa=0 sb=0 sd=0 mult=1 m=1
XM1b M1top V1 Vnode GND sky130_fd_pr__nfet_01v8 L=0.5 W=3 nf=1 ad='int((nf+1)/2) * W/nf * 0.29' as='int((nf+2)/2) * W/nf * 0.29'
+ pd='2*int((nf+1)/2) * (W/nf + 0.29)' ps='2*int((nf+2)/2) * (W/nf + 0.29)' nrd='0.29 / W' nrs='0.29 / W'
+ sa=0 sb=0 sd=0 mult=1 m=1
XM1c M1top V1 Vnode GND sky130_fd_pr__nfet_01v8 L=0.5 W=3 nf=1 ad='int((nf+1)/2) * W/nf * 0.29' as='int((nf+2)/2) * W/nf * 0.29'
+ pd='2*int((nf+1)/2) * (W/nf + 0.29)' ps='2*int((nf+2)/2) * (W/nf + 0.29)' nrd='0.29 / W' nrs='0.29 / W'
+ sa=0 sb=0 sd=0 mult=1 m=1
XM1d M1top V1 Vnode GND sky130_fd_pr__nfet_01v8 L=0.5 W=3 nf=1 ad='int((nf+1)/2) * W/nf * 0.29' as='int((nf+2)/2) * W/nf * 0.29'
+ pd='2*int((nf+1)/2) * (W/nf + 0.29)' ps='2*int((nf+2)/2) * (W/nf + 0.29)' nrd='0.29 / W' nrs='0.29 / W'
+ sa=0 sb=0 sd=0 mult=1 m=1
XM2a M2top V2 Vnode GND sky130_fd_pr__nfet_01v8 L=0.5 W=3 nf=1 ad='int((nf+1)/2) * W/nf * 0.29' as='int((nf+2)/2) * W/nf * 0.29'
+ pd='2*int((nf+1)/2) * (W/nf + 0.29)' ps='2*int((nf+2)/2) * (W/nf + 0.29)' nrd='0.29 / W' nrs='0.29 / W'
+ sa=0 sb=0 sd=0 mult=1 m=1
XM2b M2top V2 Vnode GND sky130_fd_pr__nfet_01v8 L=0.5 W=3 nf=1 ad='int((nf+1)/2) * W/nf * 0.29' as='int((nf+2)/2) * W/nf * 0.29'
+ pd='2*int((nf+1)/2) * (W/nf + 0.29)' ps='2*int((nf+2)/2) * (W/nf + 0.29)' nrd='0.29 / W' nrs='0.29 / W'
+ sa=0 sb=0 sd=0 mult=1 m=1
XM2c M2top V2 Vnode GND sky130_fd_pr__nfet_01v8 L=0.5 W=3 nf=1 ad='int((nf+1)/2) * W/nf * 0.29' as='int((nf+2)/2) * W/nf * 0.29'
+ pd='2*int((nf+1)/2) * (W/nf + 0.29)' ps='2*int((nf+2)/2) * (W/nf + 0.29)' nrd='0.29 / W' nrs='0.29 / W'
+ sa=0 sb=0 sd=0 mult=1 m=1
XM2d M2top V2 Vnode GND sky130_fd_pr__nfet_01v8 L=0.5 W=3 nf=1 ad='int((nf+1)/2) * W/nf * 0.29' as='int((nf+2)/2) * W/nf * 0.29'
+ pd='2*int((nf+1)/2) * (W/nf + 0.29)' ps='2*int((nf+2)/2) * (W/nf + 0.29)' nrd='0.29 / W' nrs='0.29 / W'
+ sa=0 sb=0 sd=0 mult=1 m=1
XMba Vnode Vb VN GND sky130_fd_pr__nfet_01v8 L=0.5 W=1.5 nf=1 ad='int((nf+1)/2) * W/nf * 0.29' as='int((nf+2)/2) * W/nf * 0.29'
+ pd='2*int((nf+1)/2) * (W/nf + 0.29)' ps='2*int((nf+2)/2) * (W/nf + 0.29)' nrd='0.29 / W' nrs='0.29 / W'
+ sa=0 sb=0 sd=0 mult=1 m=1
XMbb Vnode Vb VN GND sky130_fd_pr__nfet_01v8 L=0.5 W=1.5 nf=1 ad='int((nf+1)/2) * W/nf * 0.29' as='int((nf+2)/2) * W/nf * 0.29'
+ pd='2*int((nf+1)/2) * (W/nf + 0.29)' ps='2*int((nf+2)/2) * (W/nf + 0.29)' nrd='0.29 / W' nrs='0.29 / W'
+ sa=0 sb=0 sd=0 mult=1 m=1
XMbc Vnode Vb VN GND sky130_fd_pr__nfet_01v8 L=0.5 W=1.5 nf=1 ad='int((nf+1)/2) * W/nf * 0.29' as='int((nf+2)/2) * W/nf * 0.29'
+ pd='2*int((nf+1)/2) * (W/nf + 0.29)' ps='2*int((nf+2)/2) * (W/nf + 0.29)' nrd='0.29 / W' nrs='0.29 / W'
+ sa=0 sb=0 sd=0 mult=1 m=1
XMbd Vnode Vb VN GND sky130_fd_pr__nfet_01v8 L=0.5 W=1.5 nf=1 ad='int((nf+1)/2) * W/nf * 0.29' as='int((nf+2)/2) * W/nf * 0.29'
+ pd='2*int((nf+1)/2) * (W/nf + 0.29)' ps='2*int((nf+2)/2) * (W/nf + 0.29)' nrd='0.29 / W' nrs='0.29 / W'
+ sa=0 sb=0 sd=0 mult=1 m=1
XMbe Vnode Vb VN GND sky130_fd_pr__nfet_01v8 L=0.5 W=1.5 nf=1 ad='int((nf+1)/2) * W/nf * 0.29' as='int((nf+2)/2) * W/nf * 0.29'
+ pd='2*int((nf+1)/2) * (W/nf + 0.29)' ps='2*int((nf+2)/2) * (W/nf + 0.29)' nrd='0.29 / W' nrs='0.29 / W'
+ sa=0 sb=0 sd=0 mult=1 m=1
XMbf Vnode Vb VN GND sky130_fd_pr__nfet_01v8 L=0.5 W=1.5 nf=1 ad='int((nf+1)/2) * W/nf * 0.29' as='int((nf+2)/2) * W/nf * 0.29'
+ pd='2*int((nf+1)/2) * (W/nf + 0.29)' ps='2*int((nf+2)/2) * (W/nf + 0.29)' nrd='0.29 / W' nrs='0.29 / W'
+ sa=0 sb=0 sd=0 mult=1 m=1
XMbg Vnode Vb VN GND sky130_fd_pr__nfet_01v8 L=0.5 W=1.5 nf=1 ad='int((nf+1)/2) * W/nf * 0.29' as='int((nf+2)/2) * W/nf * 0.29'
+ pd='2*int((nf+1)/2) * (W/nf + 0.29)' ps='2*int((nf+2)/2) * (W/nf + 0.29)' nrd='0.29 / W' nrs='0.29 / W'
+ sa=0 sb=0 sd=0 mult=1 m=1
XMbh Vnode Vb VN GND sky130_fd_pr__nfet_01v8 L=0.5 W=1.5 nf=1 ad='int((nf+1)/2) * W/nf * 0.29' as='int((nf+2)/2) * W/nf * 0.29'
+ pd='2*int((nf+1)/2) * (W/nf + 0.29)' ps='2*int((nf+2)/2) * (W/nf + 0.29)' nrd='0.29 / W' nrs='0.29 / W'
+ sa=0 sb=0 sd=0 mult=1 m=1
XM7a net2 Vcn net1 GND sky130_fd_pr__nfet_01v8 L=0.5 W=3 nf=1 ad='int((nf+1)/2) * W/nf * 0.29' as='int((nf+2)/2) * W/nf * 0.29'
+ pd='2*int((nf+1)/2) * (W/nf + 0.29)' ps='2*int((nf+2)/2) * (W/nf + 0.29)' nrd='0.29 / W' nrs='0.29 / W'
+ sa=0 sb=0 sd=0 mult=1 m=1
XM7b net2 Vcn net1 GND sky130_fd_pr__nfet_01v8 L=0.5 W=3 nf=1 ad='int((nf+1)/2) * W/nf * 0.29' as='int((nf+2)/2) * W/nf * 0.29'
+ pd='2*int((nf+1)/2) * (W/nf + 0.29)' ps='2*int((nf+2)/2) * (W/nf + 0.29)' nrd='0.29 / W' nrs='0.29 / W'
+ sa=0 sb=0 sd=0 mult=1 m=1
XM7c net2 Vcn net1 GND sky130_fd_pr__nfet_01v8 L=0.5 W=3 nf=1 ad='int((nf+1)/2) * W/nf * 0.29' as='int((nf+2)/2) * W/nf * 0.29'
+ pd='2*int((nf+1)/2) * (W/nf + 0.29)' ps='2*int((nf+2)/2) * (W/nf + 0.29)' nrd='0.29 / W' nrs='0.29 / W'
+ sa=0 sb=0 sd=0 mult=1 m=1
XM7d net2 Vcn net1 GND sky130_fd_pr__nfet_01v8 L=0.5 W=3 nf=1 ad='int((nf+1)/2) * W/nf * 0.29' as='int((nf+2)/2) * W/nf * 0.29'
+ pd='2*int((nf+1)/2) * (W/nf + 0.29)' ps='2*int((nf+2)/2) * (W/nf + 0.29)' nrd='0.29 / W' nrs='0.29 / W'
+ sa=0 sb=0 sd=0 mult=1 m=1
XM8a net3 Vcn Vout GND sky130_fd_pr__nfet_01v8 L=0.5 W=3 nf=1 ad='int((nf+1)/2) * W/nf * 0.29' as='int((nf+2)/2) * W/nf * 0.29'
+ pd='2*int((nf+1)/2) * (W/nf + 0.29)' ps='2*int((nf+2)/2) * (W/nf + 0.29)' nrd='0.29 / W' nrs='0.29 / W'
+ sa=0 sb=0 sd=0 mult=1 m=1
XM8b net3 Vcn Vout GND sky130_fd_pr__nfet_01v8 L=0.5 W=3 nf=1 ad='int((nf+1)/2) * W/nf * 0.29' as='int((nf+2)/2) * W/nf * 0.29'
+ pd='2*int((nf+1)/2) * (W/nf + 0.29)' ps='2*int((nf+2)/2) * (W/nf + 0.29)' nrd='0.29 / W' nrs='0.29 / W'
+ sa=0 sb=0 sd=0 mult=1 m=1
XM8c net3 Vcn Vout GND sky130_fd_pr__nfet_01v8 L=0.5 W=3 nf=1 ad='int((nf+1)/2) * W/nf * 0.29' as='int((nf+2)/2) * W/nf * 0.29'
+ pd='2*int((nf+1)/2) * (W/nf + 0.29)' ps='2*int((nf+2)/2) * (W/nf + 0.29)' nrd='0.29 / W' nrs='0.29 / W'
+ sa=0 sb=0 sd=0 mult=1 m=1
XM8d net3 Vcn Vout GND sky130_fd_pr__nfet_01v8 L=0.5 W=3 nf=1 ad='int((nf+1)/2) * W/nf * 0.29' as='int((nf+2)/2) * W/nf * 0.29'
+ pd='2*int((nf+1)/2) * (W/nf + 0.29)' ps='2*int((nf+2)/2) * (W/nf + 0.29)' nrd='0.29 / W' nrs='0.29 / W'
+ sa=0 sb=0 sd=0 mult=1 m=1
XM9a net1 net2 VN GND sky130_fd_pr__nfet_01v8 L=0.5 W=3 nf=1 ad='int((nf+1)/2) * W/nf * 0.29' as='int((nf+2)/2) * W/nf * 0.29'
+ pd='2*int((nf+1)/2) * (W/nf + 0.29)' ps='2*int((nf+2)/2) * (W/nf + 0.29)' nrd='0.29 / W' nrs='0.29 / W'
+ sa=0 sb=0 sd=0 mult=1 m=1
XM9b net1 net2 VN GND sky130_fd_pr__nfet_01v8 L=0.5 W=3 nf=1 ad='int((nf+1)/2) * W/nf * 0.29' as='int((nf+2)/2) * W/nf * 0.29'
+ pd='2*int((nf+1)/2) * (W/nf + 0.29)' ps='2*int((nf+2)/2) * (W/nf + 0.29)' nrd='0.29 / W' nrs='0.29 / W'
+ sa=0 sb=0 sd=0 mult=1 m=1
XM9c net1 net2 VN GND sky130_fd_pr__nfet_01v8 L=0.5 W=3 nf=1 ad='int((nf+1)/2) * W/nf * 0.29' as='int((nf+2)/2) * W/nf * 0.29'
+ pd='2*int((nf+1)/2) * (W/nf + 0.29)' ps='2*int((nf+2)/2) * (W/nf + 0.29)' nrd='0.29 / W' nrs='0.29 / W'
+ sa=0 sb=0 sd=0 mult=1 m=1
XM9d net1 net2 VN GND sky130_fd_pr__nfet_01v8 L=0.5 W=3 nf=1 ad='int((nf+1)/2) * W/nf * 0.29' as='int((nf+2)/2) * W/nf * 0.29'
+ pd='2*int((nf+1)/2) * (W/nf + 0.29)' ps='2*int((nf+2)/2) * (W/nf + 0.29)' nrd='0.29 / W' nrs='0.29 / W'
+ sa=0 sb=0 sd=0 mult=1 m=1
XM10a VN net2 net3 GND sky130_fd_pr__nfet_01v8 L=0.5 W=3 nf=1 ad='int((nf+1)/2) * W/nf * 0.29' as='int((nf+2)/2) * W/nf * 0.29'
+ pd='2*int((nf+1)/2) * (W/nf + 0.29)' ps='2*int((nf+2)/2) * (W/nf + 0.29)' nrd='0.29 / W' nrs='0.29 / W'
+ sa=0 sb=0 sd=0 mult=1 m=1
XM10b VN net2 net3 GND sky130_fd_pr__nfet_01v8 L=0.5 W=3 nf=1 ad='int((nf+1)/2) * W/nf * 0.29' as='int((nf+2)/2) * W/nf * 0.29'
+ pd='2*int((nf+1)/2) * (W/nf + 0.29)' ps='2*int((nf+2)/2) * (W/nf + 0.29)' nrd='0.29 / W' nrs='0.29 / W'
+ sa=0 sb=0 sd=0 mult=1 m=1
XM10c VN net2 net3 GND sky130_fd_pr__nfet_01v8 L=0.5 W=3 nf=1 ad='int((nf+1)/2) * W/nf * 0.29' as='int((nf+2)/2) * W/nf * 0.29'
+ pd='2*int((nf+1)/2) * (W/nf + 0.29)' ps='2*int((nf+2)/2) * (W/nf + 0.29)' nrd='0.29 / W' nrs='0.29 / W'
+ sa=0 sb=0 sd=0 mult=1 m=1
XM1 VN net2 net3 GND sky130_fd_pr__nfet_01v8 L=0.5 W=3 nf=1 ad='int((nf+1)/2) * W/nf * 0.29' as='int((nf+2)/2) * W/nf * 0.29'
+ pd='2*int((nf+1)/2) * (W/nf + 0.29)' ps='2*int((nf+2)/2) * (W/nf + 0.29)' nrd='0.29 / W' nrs='0.29 / W'
+ sa=0 sb=0 sd=0 mult=1 m=1
XM5a net2 Vcp M1top VDD sky130_fd_pr__pfet_01v8 L=0.5 W=8 nf=1 ad='int((nf+1)/2) * W/nf * 0.29' as='int((nf+2)/2) * W/nf * 0.29'
+ pd='2*int((nf+1)/2) * (W/nf + 0.29)' ps='2*int((nf+2)/2) * (W/nf + 0.29)' nrd='0.29 / W' nrs='0.29 / W'
+ sa=0 sb=0 sd=0 mult=1 m=1
XM5b net2 Vcp M1top VDD sky130_fd_pr__pfet_01v8 L=0.5 W=8 nf=1 ad='int((nf+1)/2) * W/nf * 0.29' as='int((nf+2)/2) * W/nf * 0.29'
+ pd='2*int((nf+1)/2) * (W/nf + 0.29)' ps='2*int((nf+2)/2) * (W/nf + 0.29)' nrd='0.29 / W' nrs='0.29 / W'
+ sa=0 sb=0 sd=0 mult=1 m=1
XM5c net2 Vcp M1top VDD sky130_fd_pr__pfet_01v8 L=0.5 W=8 nf=1 ad='int((nf+1)/2) * W/nf * 0.29' as='int((nf+2)/2) * W/nf * 0.29'
+ pd='2*int((nf+1)/2) * (W/nf + 0.29)' ps='2*int((nf+2)/2) * (W/nf + 0.29)' nrd='0.29 / W' nrs='0.29 / W'
+ sa=0 sb=0 sd=0 mult=1 m=1
XM5d net2 Vcp M1top VDD sky130_fd_pr__pfet_01v8 L=0.5 W=8 nf=1 ad='int((nf+1)/2) * W/nf * 0.29' as='int((nf+2)/2) * W/nf * 0.29'
+ pd='2*int((nf+1)/2) * (W/nf + 0.29)' ps='2*int((nf+2)/2) * (W/nf + 0.29)' nrd='0.29 / W' nrs='0.29 / W'
+ sa=0 sb=0 sd=0 mult=1 m=1
XM6a Vout Vcp M2top VDD sky130_fd_pr__pfet_01v8 L=0.5 W=8 nf=1 ad='int((nf+1)/2) * W/nf * 0.29' as='int((nf+2)/2) * W/nf * 0.29'
+ pd='2*int((nf+1)/2) * (W/nf + 0.29)' ps='2*int((nf+2)/2) * (W/nf + 0.29)' nrd='0.29 / W' nrs='0.29 / W'
+ sa=0 sb=0 sd=0 mult=1 m=1
XM6b Vout Vcp M2top VDD sky130_fd_pr__pfet_01v8 L=0.5 W=8 nf=1 ad='int((nf+1)/2) * W/nf * 0.29' as='int((nf+2)/2) * W/nf * 0.29'
+ pd='2*int((nf+1)/2) * (W/nf + 0.29)' ps='2*int((nf+2)/2) * (W/nf + 0.29)' nrd='0.29 / W' nrs='0.29 / W'
+ sa=0 sb=0 sd=0 mult=1 m=1
XM6c Vout Vcp M2top VDD sky130_fd_pr__pfet_01v8 L=0.5 W=8 nf=1 ad='int((nf+1)/2) * W/nf * 0.29' as='int((nf+2)/2) * W/nf * 0.29'
+ pd='2*int((nf+1)/2) * (W/nf + 0.29)' ps='2*int((nf+2)/2) * (W/nf + 0.29)' nrd='0.29 / W' nrs='0.29 / W'
+ sa=0 sb=0 sd=0 mult=1 m=1
XM6d Vout Vcp M2top VDD sky130_fd_pr__pfet_01v8 L=0.5 W=8 nf=1 ad='int((nf+1)/2) * W/nf * 0.29' as='int((nf+2)/2) * W/nf * 0.29'
+ pd='2*int((nf+1)/2) * (W/nf + 0.29)' ps='2*int((nf+2)/2) * (W/nf + 0.29)' nrd='0.29 / W' nrs='0.29 / W'
+ sa=0 sb=0 sd=0 mult=1 m=1
XM3a M1top Vbp VP VDD sky130_fd_pr__pfet_01v8 L=0.5 W=8 nf=1 ad='int((nf+1)/2) * W/nf * 0.29' as='int((nf+2)/2) * W/nf * 0.29'
+ pd='2*int((nf+1)/2) * (W/nf + 0.29)' ps='2*int((nf+2)/2) * (W/nf + 0.29)' nrd='0.29 / W' nrs='0.29 / W'
+ sa=0 sb=0 sd=0 mult=1 m=1
XM3b M1top Vbp VP VDD sky130_fd_pr__pfet_01v8 L=0.5 W=8 nf=1 ad='int((nf+1)/2) * W/nf * 0.29' as='int((nf+2)/2) * W/nf * 0.29'
+ pd='2*int((nf+1)/2) * (W/nf + 0.29)' ps='2*int((nf+2)/2) * (W/nf + 0.29)' nrd='0.29 / W' nrs='0.29 / W'
+ sa=0 sb=0 sd=0 mult=1 m=1
XM3c M1top Vbp VP VDD sky130_fd_pr__pfet_01v8 L=0.5 W=8 nf=1 ad='int((nf+1)/2) * W/nf * 0.29' as='int((nf+2)/2) * W/nf * 0.29'
+ pd='2*int((nf+1)/2) * (W/nf + 0.29)' ps='2*int((nf+2)/2) * (W/nf + 0.29)' nrd='0.29 / W' nrs='0.29 / W'
+ sa=0 sb=0 sd=0 mult=1 m=1
XM3d M1top Vbp VP VDD sky130_fd_pr__pfet_01v8 L=0.5 W=8 nf=1 ad='int((nf+1)/2) * W/nf * 0.29' as='int((nf+2)/2) * W/nf * 0.29'
+ pd='2*int((nf+1)/2) * (W/nf + 0.29)' ps='2*int((nf+2)/2) * (W/nf + 0.29)' nrd='0.29 / W' nrs='0.29 / W'
+ sa=0 sb=0 sd=0 mult=1 m=1
XM4a M2top Vbp VP VDD sky130_fd_pr__pfet_01v8 L=0.5 W=8 nf=1 ad='int((nf+1)/2) * W/nf * 0.29' as='int((nf+2)/2) * W/nf * 0.29'
+ pd='2*int((nf+1)/2) * (W/nf + 0.29)' ps='2*int((nf+2)/2) * (W/nf + 0.29)' nrd='0.29 / W' nrs='0.29 / W'
+ sa=0 sb=0 sd=0 mult=1 m=1
XM4b M2top Vbp VP VDD sky130_fd_pr__pfet_01v8 L=0.5 W=8 nf=1 ad='int((nf+1)/2) * W/nf * 0.29' as='int((nf+2)/2) * W/nf * 0.29'
+ pd='2*int((nf+1)/2) * (W/nf + 0.29)' ps='2*int((nf+2)/2) * (W/nf + 0.29)' nrd='0.29 / W' nrs='0.29 / W'
+ sa=0 sb=0 sd=0 mult=1 m=1
XM4c M2top Vbp VP VDD sky130_fd_pr__pfet_01v8 L=0.5 W=8 nf=1 ad='int((nf+1)/2) * W/nf * 0.29' as='int((nf+2)/2) * W/nf * 0.29'
+ pd='2*int((nf+1)/2) * (W/nf + 0.29)' ps='2*int((nf+2)/2) * (W/nf + 0.29)' nrd='0.29 / W' nrs='0.29 / W'
+ sa=0 sb=0 sd=0 mult=1 m=1
XM4d M2top Vbp VP VDD sky130_fd_pr__pfet_01v8 L=0.5 W=8 nf=1 ad='int((nf+1)/2) * W/nf * 0.29' as='int((nf+2)/2) * W/nf * 0.29'
+ pd='2*int((nf+1)/2) * (W/nf + 0.29)' ps='2*int((nf+2)/2) * (W/nf + 0.29)' nrd='0.29 / W' nrs='0.29 / W'
+ sa=0 sb=0 sd=0 mult=1 m=1
.ends

.GLOBAL VDD
.GLOBAL GND
.end
